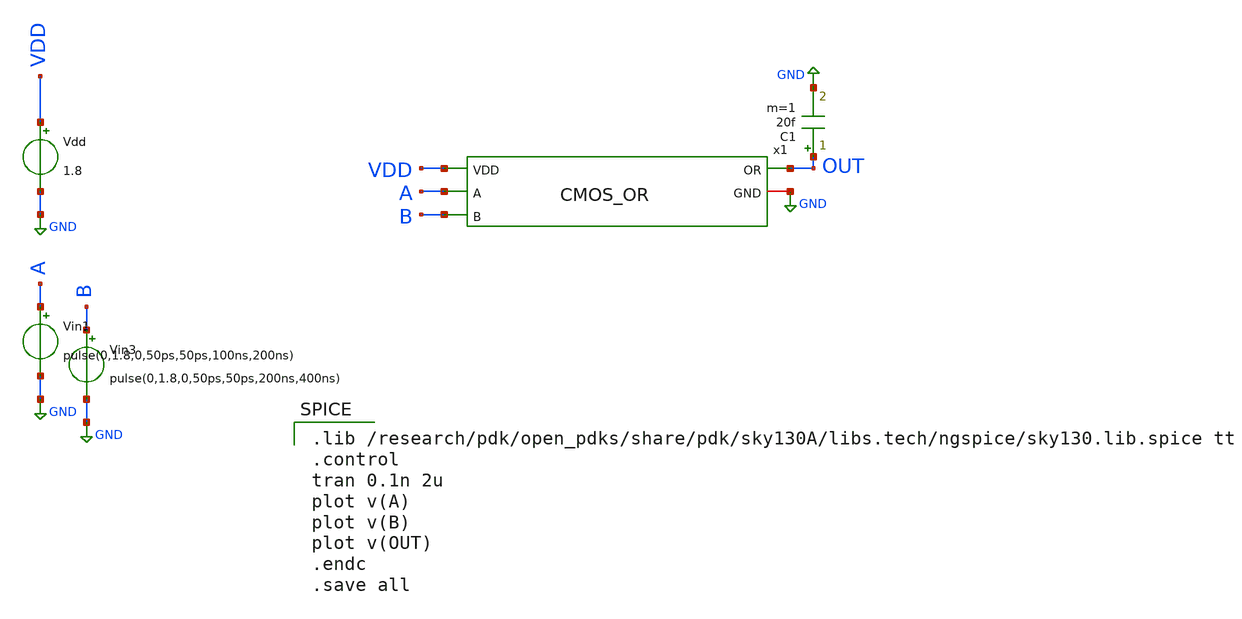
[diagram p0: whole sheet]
** sch_path: skywater_stuff/CMOS_OR_sim.sch
**.subckt CMOS_OR_sim
Vdd VDD GND 1.8
Vin1 A GND pulse(0,1.8,0,50ps,50ps,100ns,200ns)
Vin3 B GND pulse(0,1.8,0,50ps,50ps,200ns,400ns)
x1 A B OUT GND VDD CMOS_OR
C1 OUT GND 20f m=1
**** begin user architecture code

.lib /research/pdk/open_pdks/share/pdk/sky130A/libs.tech/ngspice/sky130.lib.spice tt
.control
tran 0.1n 2u
plot v(A)
plot v(B)
plot v(OUT)
.endc
.save all

**** end user architecture code
**.ends
.GLOBAL GND
.end
